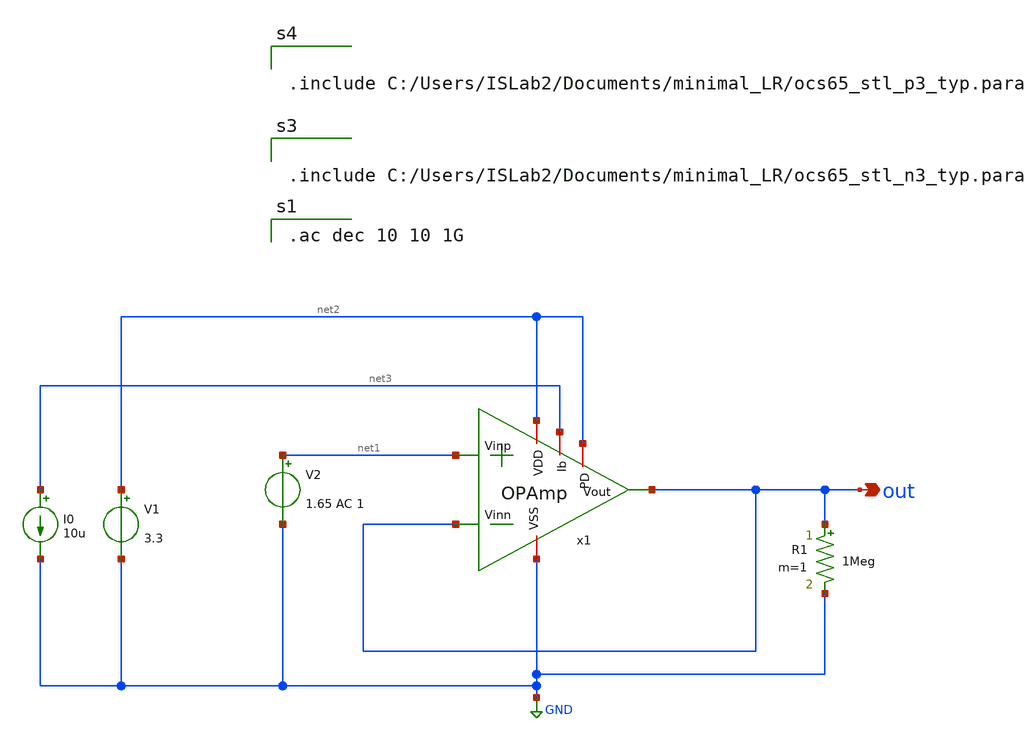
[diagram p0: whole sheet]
** sch_path: OPAmp_sim.sch
**.subckt OPAmp_sim out
*.opin out
V1 net2 GND 3.3
I0 net3 GND 10u
V2 net1 GND 1.65 AC 1
x1 net2 net3 out out net1 GND net2 OPAmp
R1 out GND 1Meg m=1
**** begin user architecture code

.ac dec 10 10 1G



.include C:/Users/ISLab2/Documents/minimal_LR/ocs65_stl_n3_typ.para



.include C:/Users/ISLab2/Documents/minimal_LR/ocs65_stl_p3_typ.para

**** end user architecture code
**.ends

* expanding   symbol:  OPAmp.sym # of pins=7
** sym_path: OPAmp.sym
** sch_path: OPAmp.sch
.subckt OPAmp VDD Ib Vout Vinn Vinp VSS PD
*.opin Vout
*.ipin Vinn
*.ipin Vinp
*.iopin Ib
*.iopin VDD
*.iopin VSS
*.iopin PD
M1 Ib Ib VDD VDD pch w=20u l=1u as=0 ps=0 ad=0 pd=0 m=1
M2 net1 Ib VDD VDD pch w=20u l=1u as=0 ps=0 ad=0 pd=0 m=1
M3 Vout Ib VDD VDD pch w=20u l=1u as=0 ps=0 ad=0 pd=0 m=10
M4 net3 net2 VSS VSS nch w=10u l=1u as=0 ps=0 ad=0 pd=0 m=1
M5 net2 Vinn net1 VDD pch w=20u l=1u as=0 ps=0 ad=0 pd=0 m=1
M6 net3 Vinp net1 VDD pch w=20u l=1u as=0 ps=0 ad=0 pd=0 m=1
M7 net2 net2 VSS VSS nch w=10u l=1u as=0 ps=0 ad=0 pd=0 m=1
M8 Vout net3 VSS VSS nch w=10u l=1u as=0 ps=0 ad=0 pd=0 m=10
C1 Vout net3 500f m=1
M9 Ib PD VDD VDD pch w=20u l=1u as=0 ps=0 ad=0 pd=0 m=1
M10 net3 net4 VSS VSS nch w=10u l=1u as=0 ps=0 ad=0 pd=0 m=1
x1 VDD net4 PD VSS INV
.ends


* expanding   symbol:  INV.sym # of pins=4
** sym_path: INV.sym
** sch_path: INV.sch
.subckt INV VDD OUT IN VSS
*.opin OUT
*.ipin IN
*.iopin VDD
*.iopin VSS
M2 OUT IN VDD VDD pch w=10u l=0.35u as=0 ps=0 ad=0 pd=0 m=1
M1 OUT IN VSS VSS nch w=5u l=0.35u as=0 ps=0 ad=0 pd=0 m=1
.ends

.GLOBAL GND
.end
